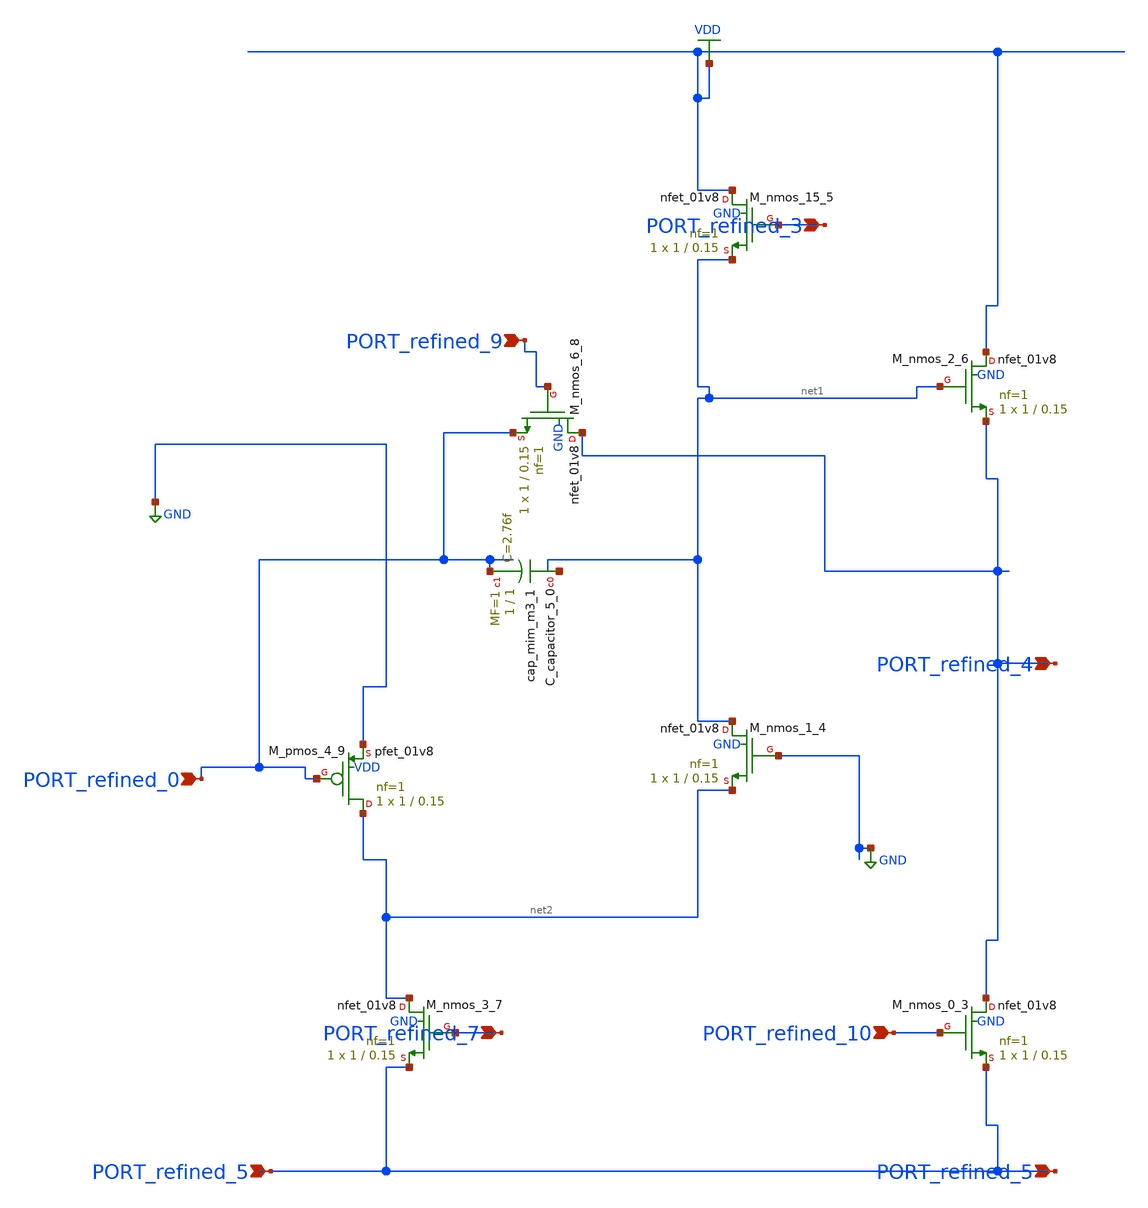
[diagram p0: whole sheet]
** sch_path: schematics/10_1016_j_nima_2022_167570_07_003.sch
**.subckt 10_1016_j_nima_2022_167570_07_003 PORT_refined_0 PORT_refined_10 PORT_refined_4
*+ PORT_refined_7 PORT_refined_5 PORT_refined_5 PORT_refined_9 PORT_refined_3
*.ipin PORT_refined_0
*.ipin PORT_refined_10
*.ipin PORT_refined_4
*.ipin PORT_refined_7
*.ipin PORT_refined_5
*.ipin PORT_refined_5
*.ipin PORT_refined_9
*.ipin PORT_refined_3
XC_capacitor_5_0 net1 PORT_refined_0 sky130_fd_pr__cap_mim_m3_1 W=1 L=1 MF=1 m=1
XM_nmos_0_3 PORT_refined_4 PORT_refined_10 PORT_refined_5 GND sky130_fd_pr__nfet_01v8 L=0.15 W=1 nf=1
+ ad='int((1 + 1)/2) * 1 / 1 * 0.29' as='int((1 + 2)/2) * 1 / 1 * 0.29' pd='2*int((1 + 1)/2) * (1 / 1 + 0.29)'
+ ps='2*int((1 + 2)/2) * (1 / 1 + 0.29)' nrd='0.29 / 1 ' nrs='0.29 / 1 ' sa=0 sb=0 sd=0 mult=1 m=1
XM_nmos_1_4 net1 GND net2 GND sky130_fd_pr__nfet_01v8 L=0.15 W=1 nf=1 ad='int((1 + 1)/2) * 1 / 1 * 0.29'
+ as='int((1 + 2)/2) * 1 / 1 * 0.29' pd='2*int((1 + 1)/2) * (1 / 1 + 0.29)' ps='2*int((1 + 2)/2) * (1 / 1 + 0.29)'
+ nrd='0.29 / 1 ' nrs='0.29 / 1 ' sa=0 sb=0 sd=0 mult=1 m=1
XM_nmos_15_5 VDD PORT_refined_3 net1 GND sky130_fd_pr__nfet_01v8 L=0.15 W=1 nf=1 ad='int((1 + 1)/2) * 1 / 1 * 0.29'
+ as='int((1 + 2)/2) * 1 / 1 * 0.29' pd='2*int((1 + 1)/2) * (1 / 1 + 0.29)' ps='2*int((1 + 2)/2) * (1 / 1 + 0.29)'
+ nrd='0.29 / 1 ' nrs='0.29 / 1 ' sa=0 sb=0 sd=0 mult=1 m=1
XM_nmos_2_6 VDD net1 PORT_refined_4 GND sky130_fd_pr__nfet_01v8 L=0.15 W=1 nf=1 ad='int((1 + 1)/2) * 1 / 1 * 0.29'
+ as='int((1 + 2)/2) * 1 / 1 * 0.29' pd='2*int((1 + 1)/2) * (1 / 1 + 0.29)' ps='2*int((1 + 2)/2) * (1 / 1 + 0.29)'
+ nrd='0.29 / 1 ' nrs='0.29 / 1 ' sa=0 sb=0 sd=0 mult=1 m=1
XM_nmos_3_7 net2 PORT_refined_7 PORT_refined_5 GND sky130_fd_pr__nfet_01v8 L=0.15 W=1 nf=1 ad='int((1 + 1)/2) * 1 / 1 * 0.29'
+ as='int((1 + 2)/2) * 1 / 1 * 0.29' pd='2*int((1 + 1)/2) * (1 / 1 + 0.29)' ps='2*int((1 + 2)/2) * (1 / 1 + 0.29)'
+ nrd='0.29 / 1 ' nrs='0.29 / 1 ' sa=0 sb=0 sd=0 mult=1 m=1
XM_nmos_6_8 PORT_refined_4 PORT_refined_9 PORT_refined_0 GND sky130_fd_pr__nfet_01v8 L=0.15 W=1 nf=1
+ ad='int((1 + 1)/2) * 1 / 1 * 0.29' as='int((1 + 2)/2) * 1 / 1 * 0.29' pd='2*int((1 + 1)/2) * (1 / 1 + 0.29)'
+ ps='2*int((1 + 2)/2) * (1 / 1 + 0.29)' nrd='0.29 / 1 ' nrs='0.29 / 1 ' sa=0 sb=0 sd=0 mult=1 m=1
XM_pmos_4_9 net2 PORT_refined_0 GND VDD sky130_fd_pr__pfet_01v8 L=0.15 W=1 nf=1 ad='int((1 + 1)/2) * 1 / 1 * 0.29'
+ as='int((1 + 2)/2) * 1 / 1 * 0.29' pd='2*int((1 + 1)/2) * (1 / 1 + 0.29)' ps='2*int((1 + 2)/2) * (1 / 1 + 0.29)'
+ nrd='0.29 / 1 ' nrs='0.29 / 1 ' sa=0 sb=0 sd=0 mult=1 m=1
**.ends
.GLOBAL GND
.GLOBAL VDD
.end
